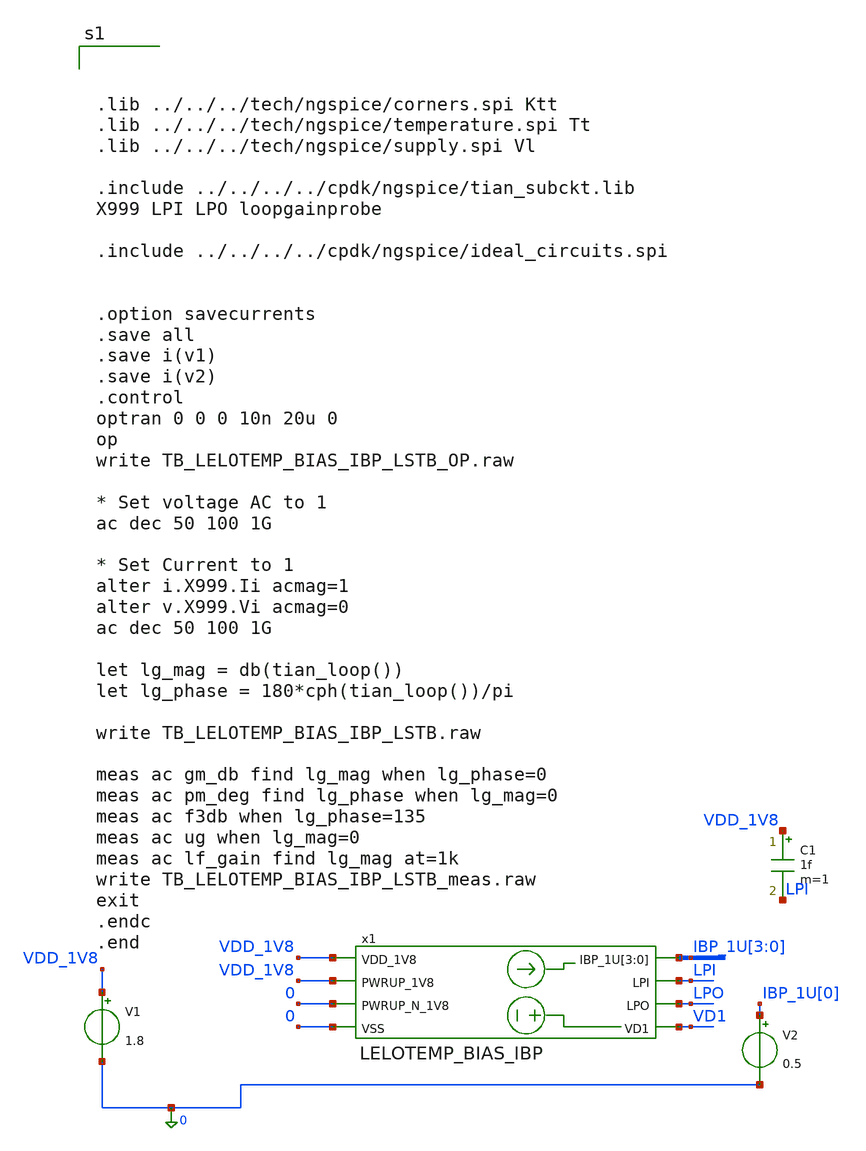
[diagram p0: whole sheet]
** sch_path: design/LELO_TEMP_SKY130A/TB_LELOTEMP_BIAS_IBP_LSTB.sch
**.subckt TB_LELOTEMP_BIAS_IBP_LSTB
V1 VDD_1V8 0 1.8
V2 IBP_1U[0] 0 0.5
x1 VDD_1V8 LPI IBP_1U[3] IBP_1U[2] IBP_1U[1] IBP_1U[0] LPO VD1 VDD_1V8 0 0 LELOTEMP_BIAS_IBP
C1 VDD_1V8 LPI 1f m=1
**** begin user architecture code



.lib ../../../tech/ngspice/corners.spi Ktt
.lib ../../../tech/ngspice/temperature.spi Tt
.lib ../../../tech/ngspice/supply.spi Vl

.include ../../../../cpdk/ngspice/tian_subckt.lib
X999 LPI LPO loopgainprobe

.include ../../../../cpdk/ngspice/ideal_circuits.spi


.option savecurrents
.save all
.save i(v1)
.save i(v2)
.control
optran 0 0 0 10n 20u 0
op
write TB_LELOTEMP_BIAS_IBP_LSTB_OP.raw

* Set voltage AC to 1
ac dec 50 100 1G

* Set Current to 1
alter i.X999.Ii acmag=1
alter v.X999.Vi acmag=0
ac dec 50 100 1G

let lg_mag = db(tian_loop())
let lg_phase = 180*cph(tian_loop())/pi

write TB_LELOTEMP_BIAS_IBP_LSTB.raw

meas ac gm_db find lg_mag when lg_phase=0
meas ac pm_deg find lg_phase when lg_mag=0
meas ac f3db when lg_phase=135
meas ac ug when lg_mag=0
meas ac lf_gain find lg_mag at=1k
write TB_LELOTEMP_BIAS_IBP_LSTB_meas.raw
exit
.endc
.end



**** end user architecture code
**.ends
.end
